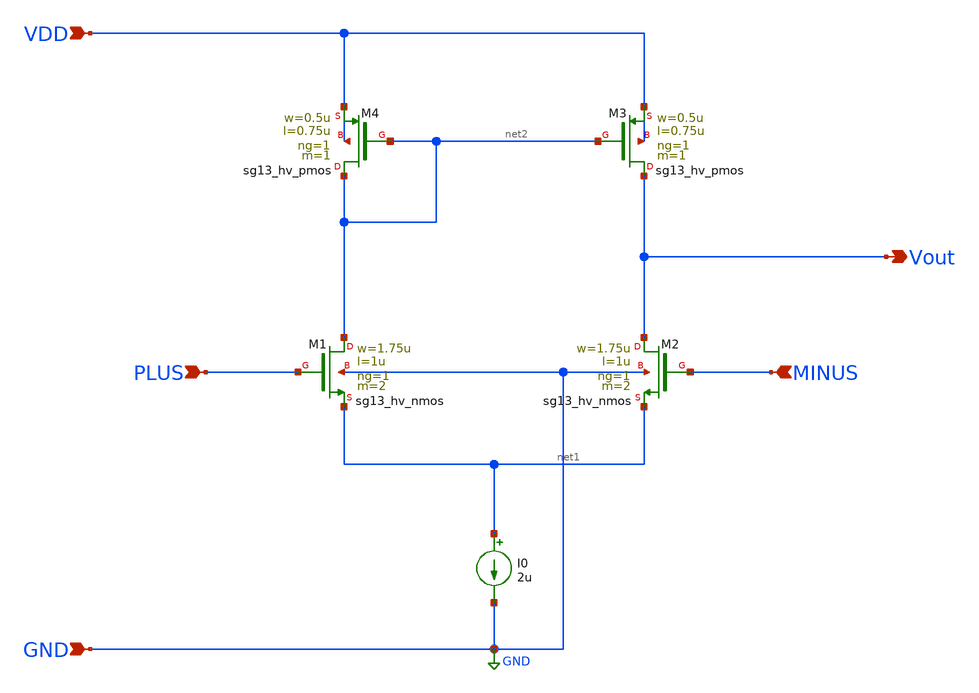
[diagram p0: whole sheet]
** sch_path: Design Files/RAMP/OTA/NOTA.sch
**.subckt NOTA VDD GND PLUS MINUS Vout
*.ipin VDD
*.ipin GND
*.ipin PLUS
*.ipin MINUS
*.opin Vout
XM1 net2 PLUS net1 GND sg13_hv_nmos w=1.75u l=1u ng=1 m=2 mm_ok=1
XM2 Vout MINUS net1 GND sg13_hv_nmos w=1.75u l=1u ng=1 m=2 mm_ok=1
I0 net1 GND 2u
XM3 Vout net2 VDD VDD sg13_hv_pmos w=0.5u l=0.75u ng=1 m=1 mm_ok=1
XM4 net2 net2 VDD VDD sg13_hv_pmos w=0.5u l=0.75u ng=1 m=1 mm_ok=1
**.ends
.GLOBAL GND
.end
